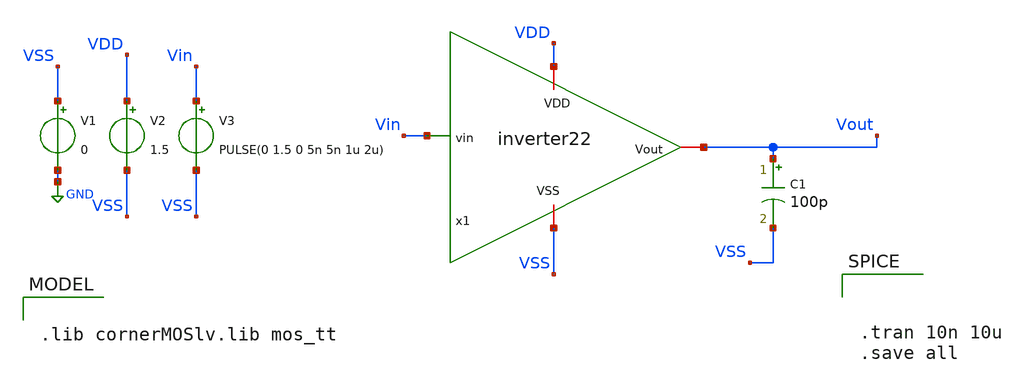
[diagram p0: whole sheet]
** sch_path: Lab2/inverter22_tb_tran.sch
**.subckt inverter22_tb_tran
x1 VDD Vin Vout VSS inverter22
V1 VSS GND 0
V2 VDD VSS 1.5
V3 Vin VSS PULSE(0 1.5 0 5n 5n 1u 2u)
C1 Vout VSS 100p m=1
**** begin user architecture code

.lib cornerMOSlv.lib mos_tt




.tran 10n 10u
.save all



**** end user architecture code
**.ends

* expanding   symbol:
*+  /home/fcastellanos/Documents/SEED_Bootcamp_ihp/Modulo_Analogico/Lab2/inverter22.sym # of pins=4
** sym_path: Lab2/inverter22.sym
** sch_path: Lab2/inverter22.sch
.subckt inverter22 VDD vin Vout VSS
*.ipin vin
*.iopin Vout
*.iopin VDD
*.iopin VSS
XM1 Vout vin VSS VSS sg13_lv_nmos w=1u l=1u ng=1 m=1 mm_ok=1
XM2 Vout vin VDD VDD sg13_lv_pmos w=3u l=1u ng=1 m=1 rfmode=1 mm_ok=1
.ends

.GLOBAL GND
.end
